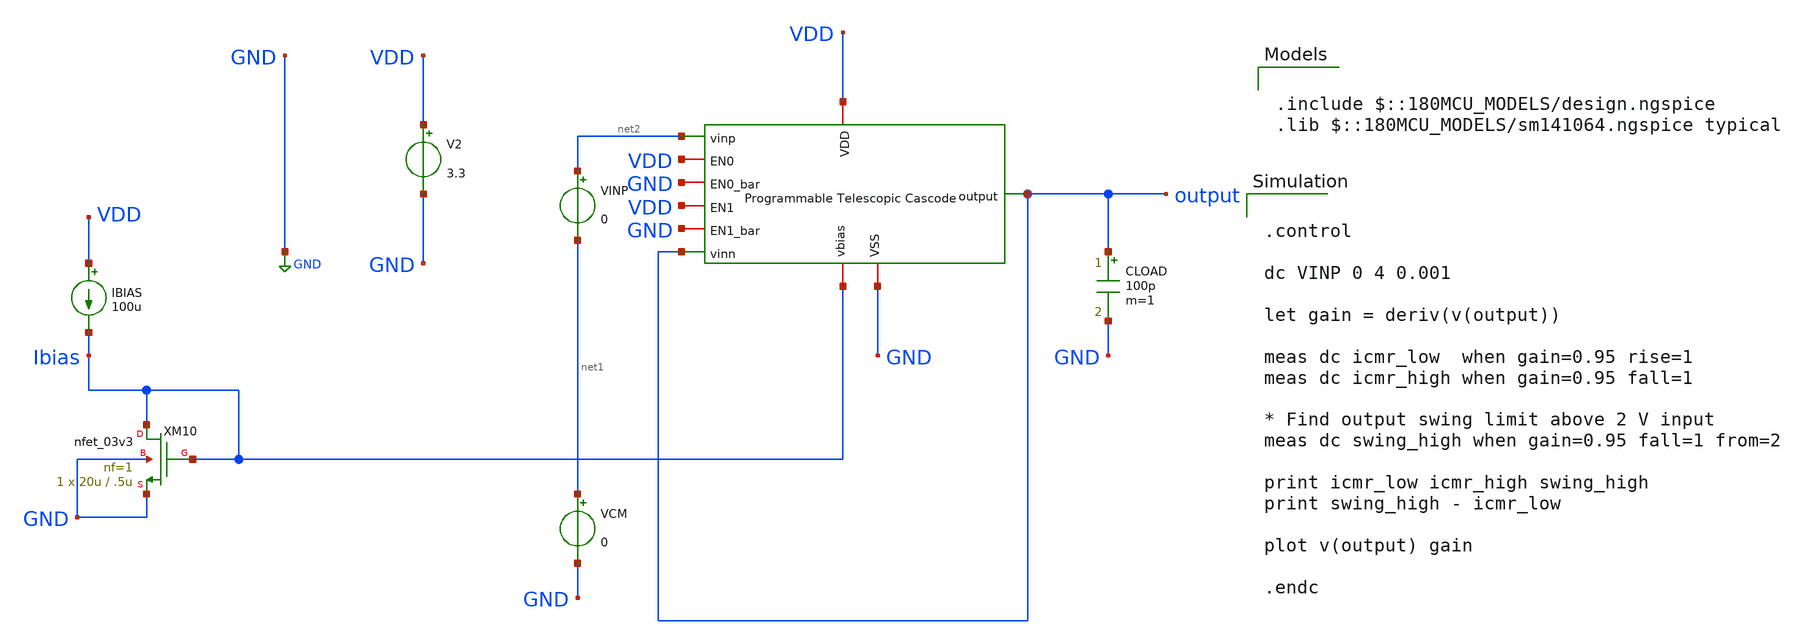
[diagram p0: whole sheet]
** sch_path: designs/libs/core_amps/ota_telescopic/programmable tb/programmable_telescopic_cascode_dc_unity.sch
**.subckt programmable_telescopic_cascode_dc_unity
V2 VDD GND 3.3
CLOAD output GND 100p m=1
VINP net2 net1 0
VCM net1 GND 0
x1 VDD output VDD GND VDD GND output net2 GND Ibias programmable_telescopic_cascode
IBIAS VDD Ibias 100u
XM10 Ibias Ibias GND GND nfet_03v3 L=.5u W=20u nf=1 ad='int((nf+1)/2) * W/nf * 0.18u' as='int((nf+2)/2) * W/nf * 0.18u'
+ pd='2*int((nf+1)/2) * (W/nf + 0.18u)' ps='2*int((nf+2)/2) * (W/nf + 0.18u)' nrd='0.18u / W' nrs='0.18u / W'
+ sa=0 sb=0 sd=0 m=1
**** begin user architecture code

.include $::180MCU_MODELS/design.ngspice
.lib $::180MCU_MODELS/sm141064.ngspice typical



.control

dc VINP 0 4 0.001

let gain = deriv(v(output))

meas dc icmr_low  when gain=0.95 rise=1
meas dc icmr_high when gain=0.95 fall=1

* Find output swing limit above 2 V input
meas dc swing_high when gain=0.95 fall=1 from=2

print icmr_low icmr_high swing_high
print swing_high - icmr_low

plot v(output) gain

.endc


**** end user architecture code
**.ends
.GLOBAL GND
.end
